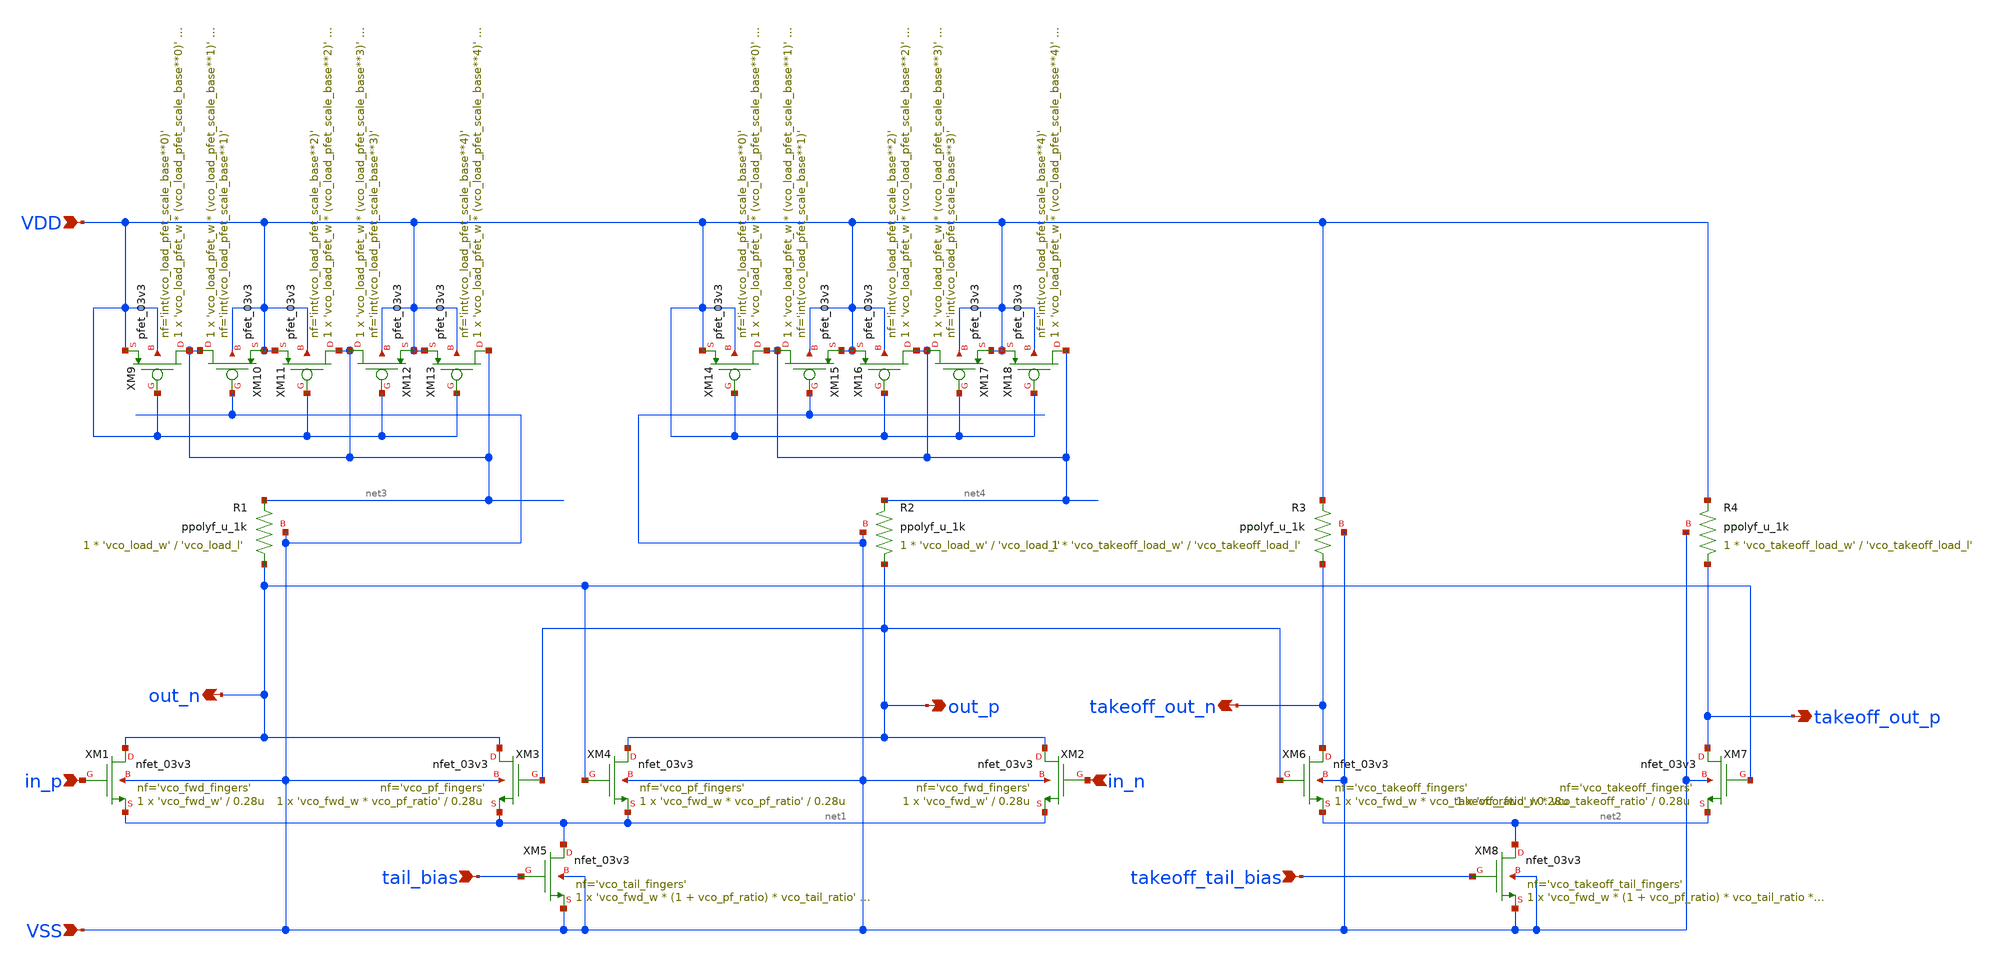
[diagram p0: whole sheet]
** sch_path: xschem/vco_core_segment.sch
**.subckt vco_core_segment VSS VDD out_n out_p in_p in_n takeoff_out_n takeoff_out_p tail_bias
*+ takeoff_tail_bias
*.ipin VSS
*.ipin VDD
*.opin out_n
*.opin out_p
*.ipin in_p
*.ipin in_n
*.opin takeoff_out_n
*.opin takeoff_out_p
*.ipin tail_bias
*.ipin takeoff_tail_bias
XM1 out_n in_p net1 VSS nfet_03v3 L=0.28u W='vco_fwd_w' nf='vco_fwd_fingers' ad='int((nf+1)/2) * W/nf * 0.18u'
+ as='int((nf+2)/2) * W/nf * 0.18u' pd='2*int((nf+1)/2) * (W/nf + 0.18u)' ps='2*int((nf+2)/2) * (W/nf + 0.18u)'
+ nrd='0.18u / W' nrs='0.18u / W' sa=0 sb=0 sd=0 m=1
XM3 out_n out_p net1 VSS nfet_03v3 L=0.28u W='vco_fwd_w * vco_pf_ratio' nf='vco_pf_fingers' ad='int((nf+1)/2) * W/nf * 0.18u'
+ as='int((nf+2)/2) * W/nf * 0.18u' pd='2*int((nf+1)/2) * (W/nf + 0.18u)' ps='2*int((nf+2)/2) * (W/nf + 0.18u)'
+ nrd='0.18u / W' nrs='0.18u / W' sa=0 sb=0 sd=0 m=1
XM4 out_p out_n net1 VSS nfet_03v3 L=0.28u W='vco_fwd_w * vco_pf_ratio' nf='vco_pf_fingers' ad='int((nf+1)/2) * W/nf * 0.18u'
+ as='int((nf+2)/2) * W/nf * 0.18u' pd='2*int((nf+1)/2) * (W/nf + 0.18u)' ps='2*int((nf+2)/2) * (W/nf + 0.18u)'
+ nrd='0.18u / W' nrs='0.18u / W' sa=0 sb=0 sd=0 m=1
XM5 net1 tail_bias VSS VSS nfet_03v3 L='vco_tail_l' W='vco_fwd_w * (1 + vco_pf_ratio) * vco_tail_ratio'
+ nf='vco_tail_fingers' ad='int((nf+1)/2) * W/nf * 0.18u' as='int((nf+2)/2) * W/nf * 0.18u' pd='2*int((nf+1)/2) * (W/nf + 0.18u)'
+ ps='2*int((nf+2)/2) * (W/nf + 0.18u)' nrd='0.18u / W' nrs='0.18u / W' sa=0 sb=0 sd=0 m=1
XM2 out_p in_n net1 VSS nfet_03v3 L=0.28u W='vco_fwd_w' nf='vco_fwd_fingers' ad='int((nf+1)/2) * W/nf * 0.18u'
+ as='int((nf+2)/2) * W/nf * 0.18u' pd='2*int((nf+1)/2) * (W/nf + 0.18u)' ps='2*int((nf+2)/2) * (W/nf + 0.18u)'
+ nrd='0.18u / W' nrs='0.18u / W' sa=0 sb=0 sd=0 m=1
XR1 out_n net3 VSS ppolyf_u_1k r_width='vco_load_w' r_length='vco_load_l' m=1
XR2 out_p net4 VSS ppolyf_u_1k r_width='vco_load_w' r_length='vco_load_l' m=1
XM6 takeoff_out_n out_p net2 VSS nfet_03v3 L=0.28u W='vco_fwd_w * vco_takeoff_ratio' nf='vco_takeoff_fingers'
+ ad='int((nf+1)/2) * W/nf * 0.18u' as='int((nf+2)/2) * W/nf * 0.18u' pd='2*int((nf+1)/2) * (W/nf + 0.18u)'
+ ps='2*int((nf+2)/2) * (W/nf + 0.18u)' nrd='0.18u / W' nrs='0.18u / W' sa=0 sb=0 sd=0 m=1
XM7 takeoff_out_p out_n net2 VSS nfet_03v3 L=0.28u W='vco_fwd_w * vco_takeoff_ratio' nf='vco_takeoff_fingers'
+ ad='int((nf+1)/2) * W/nf * 0.18u' as='int((nf+2)/2) * W/nf * 0.18u' pd='2*int((nf+1)/2) * (W/nf + 0.18u)'
+ ps='2*int((nf+2)/2) * (W/nf + 0.18u)' nrd='0.18u / W' nrs='0.18u / W' sa=0 sb=0 sd=0 m=1
XM8 net2 takeoff_tail_bias VSS VSS nfet_03v3 L='vco_takeoff_tail_l' W='vco_fwd_w * (1 + vco_pf_ratio) * vco_tail_ratio * vco_takeoff_ratio'
+ nf='vco_takeoff_tail_fingers' ad='int((nf+1)/2) * W/nf * 0.18u' as='int((nf+2)/2) * W/nf * 0.18u' pd='2*int((nf+1)/2) * (W/nf + 0.18u)'
+ ps='2*int((nf+2)/2) * (W/nf + 0.18u)' nrd='0.18u / W' nrs='0.18u / W' sa=0 sb=0 sd=0 m=1
XR3 takeoff_out_n VDD VSS ppolyf_u_1k r_width='vco_takeoff_load_w' r_length='vco_takeoff_load_l' m=1
XR4 takeoff_out_p VDD VSS ppolyf_u_1k r_width='vco_takeoff_load_w' r_length='vco_takeoff_load_l' m=1
XM9 net3 VDD VDD VDD pfet_03v3 L='vco_load_pfet_l' W='vco_load_pfet_w * (vco_load_pfet_scale_base**0)'
+ nf='int(vco_load_pfet_scale_base**0)' ad='int((nf+1)/2) * W/nf * 0.18u' as='int((nf+2)/2) * W/nf * 0.18u'
+ pd='2*int((nf+1)/2) * (W/nf + 0.18u)' ps='2*int((nf+2)/2) * (W/nf + 0.18u)' nrd='0.18u / W' nrs='0.18u / W'
+ sa=0 sb=0 sd=0 m=1
XM10 net3 VSS VDD VDD pfet_03v3 L='vco_load_pfet_l' W='vco_load_pfet_w * (vco_load_pfet_scale_base**1)'
+ nf='int(vco_load_pfet_scale_base**1)' ad='int((nf+1)/2) * W/nf * 0.18u' as='int((nf+2)/2) * W/nf * 0.18u'
+ pd='2*int((nf+1)/2) * (W/nf + 0.18u)' ps='2*int((nf+2)/2) * (W/nf + 0.18u)' nrd='0.18u / W' nrs='0.18u / W'
+ sa=0 sb=0 sd=0 m=1
XM11 net3 VDD VDD VDD pfet_03v3 L='vco_load_pfet_l' W='vco_load_pfet_w * (vco_load_pfet_scale_base**2)'
+ nf='int(vco_load_pfet_scale_base**2)' ad='int((nf+1)/2) * W/nf * 0.18u' as='int((nf+2)/2) * W/nf * 0.18u'
+ pd='2*int((nf+1)/2) * (W/nf + 0.18u)' ps='2*int((nf+2)/2) * (W/nf + 0.18u)' nrd='0.18u / W' nrs='0.18u / W'
+ sa=0 sb=0 sd=0 m=1
XM12 net3 VDD VDD VDD pfet_03v3 L='vco_load_pfet_l' W='vco_load_pfet_w * (vco_load_pfet_scale_base**3)'
+ nf='int(vco_load_pfet_scale_base**3)' ad='int((nf+1)/2) * W/nf * 0.18u' as='int((nf+2)/2) * W/nf * 0.18u'
+ pd='2*int((nf+1)/2) * (W/nf + 0.18u)' ps='2*int((nf+2)/2) * (W/nf + 0.18u)' nrd='0.18u / W' nrs='0.18u / W'
+ sa=0 sb=0 sd=0 m=1
XM13 net3 VDD VDD VDD pfet_03v3 L='vco_load_pfet_l' W='vco_load_pfet_w * (vco_load_pfet_scale_base**4)'
+ nf='int(vco_load_pfet_scale_base**4)' ad='int((nf+1)/2) * W/nf * 0.18u' as='int((nf+2)/2) * W/nf * 0.18u'
+ pd='2*int((nf+1)/2) * (W/nf + 0.18u)' ps='2*int((nf+2)/2) * (W/nf + 0.18u)' nrd='0.18u / W' nrs='0.18u / W'
+ sa=0 sb=0 sd=0 m=1
XM14 net4 VDD VDD VDD pfet_03v3 L='vco_load_pfet_l' W='vco_load_pfet_w * (vco_load_pfet_scale_base**0)'
+ nf='int(vco_load_pfet_scale_base**0)' ad='int((nf+1)/2) * W/nf * 0.18u' as='int((nf+2)/2) * W/nf * 0.18u'
+ pd='2*int((nf+1)/2) * (W/nf + 0.18u)' ps='2*int((nf+2)/2) * (W/nf + 0.18u)' nrd='0.18u / W' nrs='0.18u / W'
+ sa=0 sb=0 sd=0 m=1
XM15 net4 VSS VDD VDD pfet_03v3 L='vco_load_pfet_l' W='vco_load_pfet_w * (vco_load_pfet_scale_base**1)'
+ nf='int(vco_load_pfet_scale_base**1)' ad='int((nf+1)/2) * W/nf * 0.18u' as='int((nf+2)/2) * W/nf * 0.18u'
+ pd='2*int((nf+1)/2) * (W/nf + 0.18u)' ps='2*int((nf+2)/2) * (W/nf + 0.18u)' nrd='0.18u / W' nrs='0.18u / W'
+ sa=0 sb=0 sd=0 m=1
XM16 net4 VDD VDD VDD pfet_03v3 L='vco_load_pfet_l' W='vco_load_pfet_w * (vco_load_pfet_scale_base**2)'
+ nf='int(vco_load_pfet_scale_base**2)' ad='int((nf+1)/2) * W/nf * 0.18u' as='int((nf+2)/2) * W/nf * 0.18u'
+ pd='2*int((nf+1)/2) * (W/nf + 0.18u)' ps='2*int((nf+2)/2) * (W/nf + 0.18u)' nrd='0.18u / W' nrs='0.18u / W'
+ sa=0 sb=0 sd=0 m=1
XM17 net4 VDD VDD VDD pfet_03v3 L='vco_load_pfet_l' W='vco_load_pfet_w * (vco_load_pfet_scale_base**3)'
+ nf='int(vco_load_pfet_scale_base**3)' ad='int((nf+1)/2) * W/nf * 0.18u' as='int((nf+2)/2) * W/nf * 0.18u'
+ pd='2*int((nf+1)/2) * (W/nf + 0.18u)' ps='2*int((nf+2)/2) * (W/nf + 0.18u)' nrd='0.18u / W' nrs='0.18u / W'
+ sa=0 sb=0 sd=0 m=1
XM18 net4 VDD VDD VDD pfet_03v3 L='vco_load_pfet_l' W='vco_load_pfet_w * (vco_load_pfet_scale_base**4)'
+ nf='int(vco_load_pfet_scale_base**4)' ad='int((nf+1)/2) * W/nf * 0.18u' as='int((nf+2)/2) * W/nf * 0.18u'
+ pd='2*int((nf+1)/2) * (W/nf + 0.18u)' ps='2*int((nf+2)/2) * (W/nf + 0.18u)' nrd='0.18u / W' nrs='0.18u / W'
+ sa=0 sb=0 sd=0 m=1
**.ends
.end
